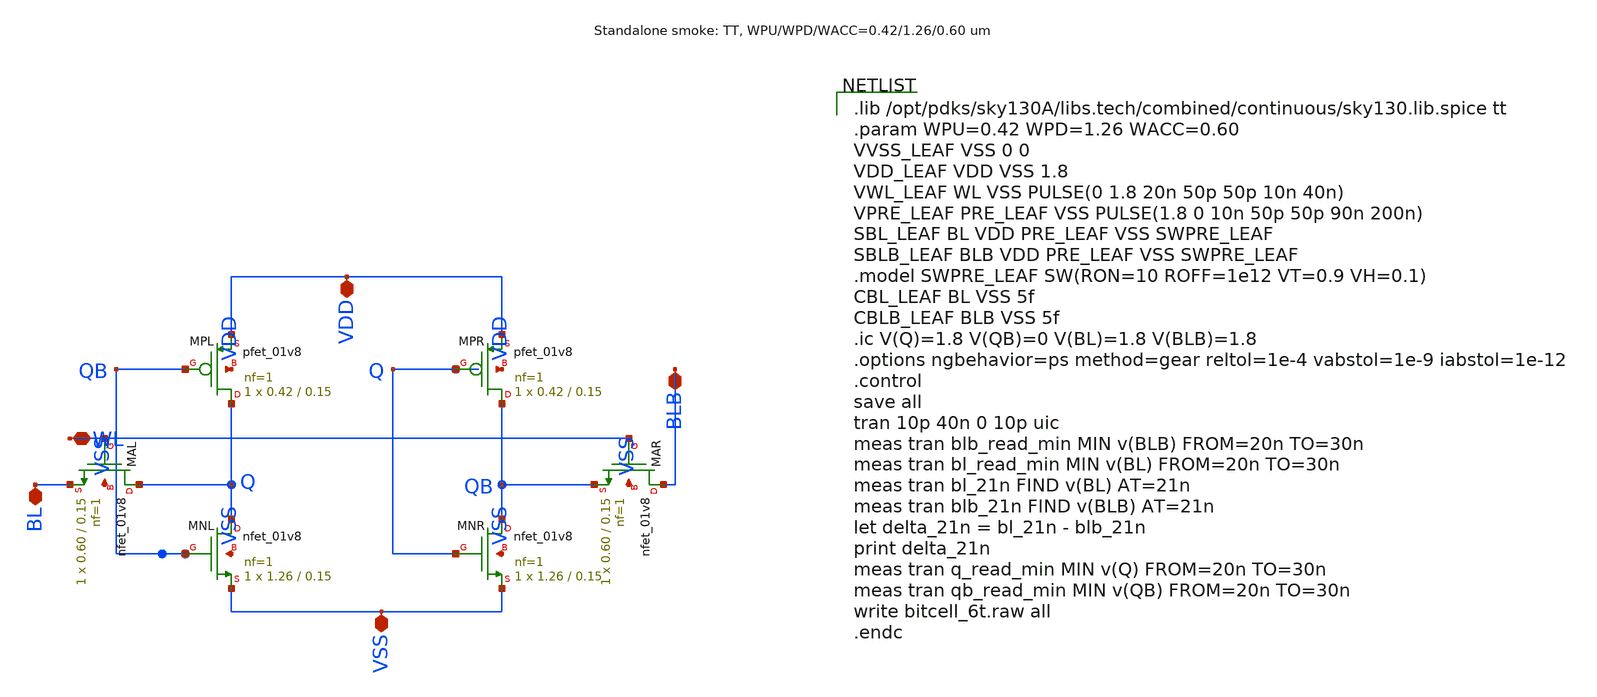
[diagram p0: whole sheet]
** sch_path: sims/integration/results/reconciliation_20261030/physical/cells/bitcell_6t/bitcell_6t.sch
**.subckt bitcell_6t VDD BL BLB VSS WL
*.iopin VDD
*.iopin BL
*.iopin BLB
*.iopin VSS
*.iopin WL
XMPL Q QB VDD VDD sky130_fd_pr__pfet_01v8 L=0.15 W=0.42 nf=1 ad='W * 0.29' as='W * 0.29' pd='W + 2 * 0.29'
+ ps='W + 2 * 0.29' nrd=0 nrs=0 sa=0 sb=0 sd=0 mult=1 m=1
XMNL Q QB VSS VSS sky130_fd_pr__nfet_01v8 L=0.15 W=1.26 nf=1 ad='W * 0.29' as='W * 0.29' pd='W + 2 * 0.29'
+ ps='W + 2 * 0.29' nrd=0 nrs=0 sa=0 sb=0 sd=0 mult=1 m=1
XMPR QB Q VDD VDD sky130_fd_pr__pfet_01v8 L=0.15 W=0.42 nf=1 ad='W * 0.29' as='W * 0.29' pd='W + 2 * 0.29'
+ ps='W + 2 * 0.29' nrd=0 nrs=0 sa=0 sb=0 sd=0 mult=1 m=1
XMNR QB Q VSS VSS sky130_fd_pr__nfet_01v8 L=0.15 W=1.26 nf=1 ad='W * 0.29' as='W * 0.29' pd='W + 2 * 0.29'
+ ps='W + 2 * 0.29' nrd=0 nrs=0 sa=0 sb=0 sd=0 mult=1 m=1
XMAL Q WL BL VSS sky130_fd_pr__nfet_01v8 L=0.15 W=0.60 nf=1 ad='W * 0.29' as='W * 0.29' pd='W + 2 * 0.29'
+ ps='W + 2 * 0.29' nrd=0 nrs=0 sa=0 sb=0 sd=0 mult=1 m=1
XMAR BLB WL QB VSS sky130_fd_pr__nfet_01v8 L=0.15 W=0.60 nf=1 ad='W * 0.29' as='W * 0.29' pd='W + 2 * 0.29'
+ ps='W + 2 * 0.29' nrd=0 nrs=0 sa=0 sb=0 sd=0 mult=1 m=1
**** begin user architecture code

.lib /opt/pdks/sky130A/libs.tech/combined/continuous/sky130.lib.spice tt
.param WPU=0.42 WPD=1.26 WACC=0.60
VVSS_LEAF VSS 0 0
VDD_LEAF VDD VSS 1.8
VWL_LEAF WL VSS PULSE(0 1.8 20n 50p 50p 10n 40n)
VPRE_LEAF PRE_LEAF VSS PULSE(1.8 0 10n 50p 50p 90n 200n)
SBL_LEAF BL VDD PRE_LEAF VSS SWPRE_LEAF
SBLB_LEAF BLB VDD PRE_LEAF VSS SWPRE_LEAF
.model SWPRE_LEAF SW(RON=10 ROFF=1e12 VT=0.9 VH=0.1)
CBL_LEAF BL VSS 5f
CBLB_LEAF BLB VSS 5f
.ic V(Q)=1.8 V(QB)=0 V(BL)=1.8 V(BLB)=1.8
.options ngbehavior=ps method=gear reltol=1e-4 vabstol=1e-9 iabstol=1e-12
.control
save all
tran 10p 40n 0 10p uic
meas tran blb_read_min MIN v(BLB) FROM=20n TO=30n
meas tran bl_read_min MIN v(BL) FROM=20n TO=30n
meas tran bl_21n FIND v(BL) AT=21n
meas tran blb_21n FIND v(BLB) AT=21n
let delta_21n = bl_21n - blb_21n
print delta_21n
meas tran q_read_min MIN v(Q) FROM=20n TO=30n
meas tran qb_read_min MIN v(QB) FROM=20n TO=30n
write bitcell_6t.raw all
.endc

**** end user architecture code
**.ends
.end
